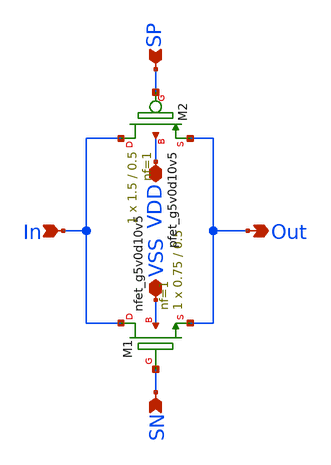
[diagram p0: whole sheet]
** sch_path: xschem/TransmissionGate.sch
**.subckt TransmissionGate Out In SP VDD VSS SN
*.opin Out
*.ipin In
*.ipin SP
*.iopin VDD
*.iopin VSS
*.ipin SN
XM1 In SN Out VSS sky130_fd_pr__nfet_g5v0d10v5 L=0.5 W=0.75 nf=1 ad='int((nf+1)/2) * W/nf * 0.29' as='int((nf+2)/2) * W/nf * 0.29'
+ pd='2*int((nf+1)/2) * (W/nf + 0.29)' ps='2*int((nf+2)/2) * (W/nf + 0.29)' nrd='0.29 / W' nrs='0.29 / W'
+ sa=0 sb=0 sd=0 mult=1 m=1
XM2 In SP Out VDD sky130_fd_pr__pfet_g5v0d10v5 L=0.5 W=1.5 nf=1 ad='int((nf+1)/2) * W/nf * 0.29' as='int((nf+2)/2) * W/nf * 0.29'
+ pd='2*int((nf+1)/2) * (W/nf + 0.29)' ps='2*int((nf+2)/2) * (W/nf + 0.29)' nrd='0.29 / W' nrs='0.29 / W'
+ sa=0 sb=0 sd=0 mult=1 m=1
**.ends
.end
